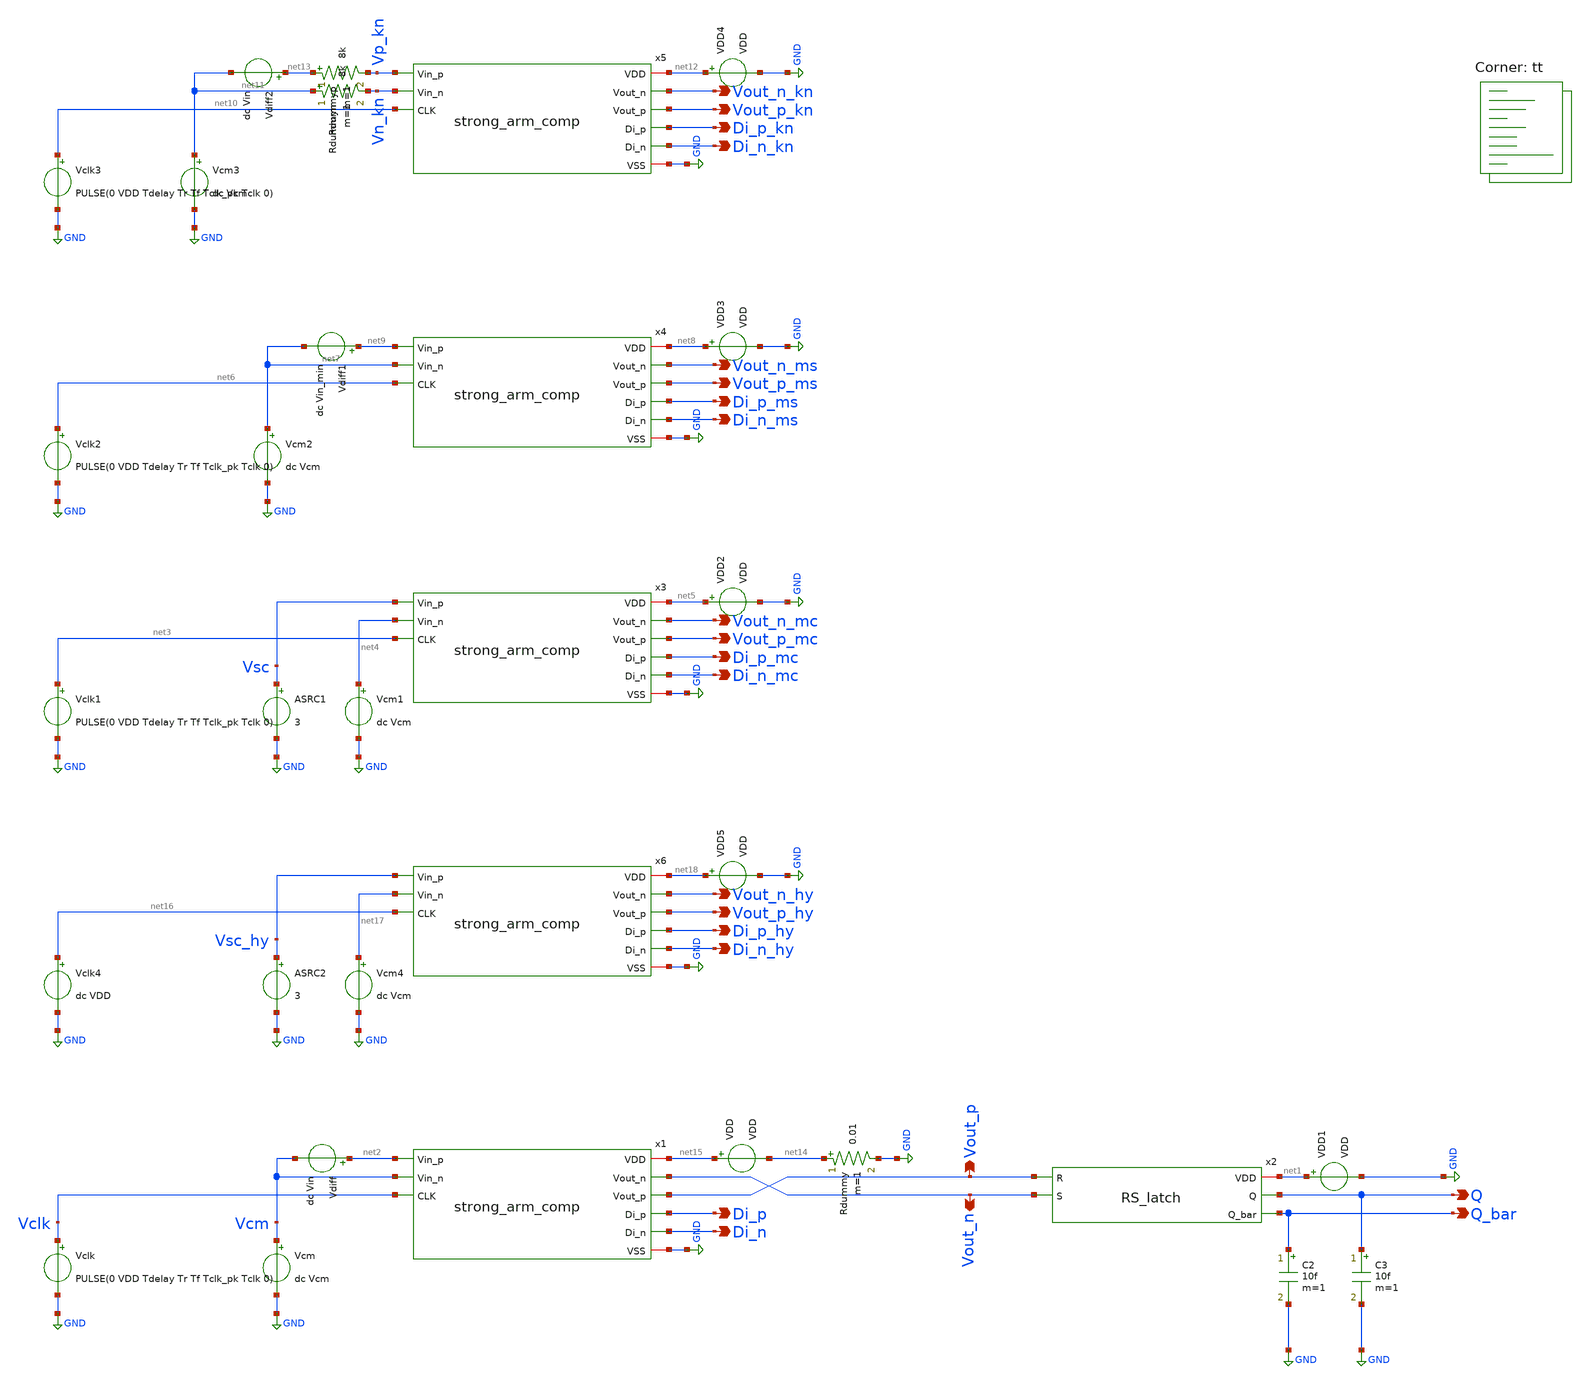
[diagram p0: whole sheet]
** sch_path: xschem/strong_arm_comp_tb.sch
**.subckt strong_arm_comp_tb Vout_n Vout_p Q Q_bar Vout_n_mc Vout_p_mc Vout_n_ms Vout_p_ms Vout_n_kn
*+ Vout_p_kn Vout_n_hy Vout_p_hy Di_p Di_n Di_p_hy Di_n_hy Di_p_ms Di_n_ms Di_p_kn Di_n_kn Di_p_mc Di_n_mc
*.opin Vout_n
*.opin Vout_p
*.opin Q
*.opin Q_bar
*.opin Vout_n_mc
*.opin Vout_p_mc
*.opin Vout_n_ms
*.opin Vout_p_ms
*.opin Vout_n_kn
*.opin Vout_p_kn
*.opin Vout_n_hy
*.opin Vout_p_hy
*.opin Di_p
*.opin Di_n
*.opin Di_p_hy
*.opin Di_n_hy
*.opin Di_p_ms
*.opin Di_n_ms
*.opin Di_p_kn
*.opin Di_n_kn
*.opin Di_p_mc
*.opin Di_n_mc
VDD net15 net14 VDD
Vclk Vclk GND PULSE(0 VDD Tdelay Tr Tf Tclk_pk Tclk 0)
Vcm Vcm GND dc Vcm
Vdiff net2 Vcm dc Vin
C2 Q_bar GND 10f m=1
C3 Q GND 10f m=1
Rdummy net14 GND 0.01 m=1
VDD1 net1 GND VDD
x1 net15 Vout_n Vout_p Di_p Di_n net2 Vcm Vclk GND strong_arm_comp
VDD2 net5 GND VDD
Vclk1 net3 GND PULSE(0 VDD Tdelay Tr Tf Tclk_pk Tclk 0)
Vcm1 net4 GND dc Vcm
x3 net5 Vout_n_mc Vout_p_mc Di_p_mc Di_n_mc Vsc net4 net3 GND strong_arm_comp
ASRC1 %v([ Vsc ]) filesrc
VDD3 net8 GND VDD
Vclk2 net6 GND PULSE(0 VDD Tdelay Tr Tf Tclk_pk Tclk 0)
Vcm2 net7 GND dc Vcm
x4 net8 Vout_n_ms Vout_p_ms Di_p_ms Di_n_ms net9 net7 net6 GND strong_arm_comp
Vdiff1 net9 net7 dc Vin_min
VDD4 net12 GND VDD
Vclk3 net10 GND PULSE(0 VDD Tdelay Tr Tf Tclk_pk Tclk 0)
Vcm3 net11 GND dc Vcm
x5 net12 Vout_n_kn Vout_p_kn Di_p_kn Di_n_kn Vp_kn Vn_kn net10 GND strong_arm_comp
Vdiff2 net13 net11 dc Vin
Rdummyp net13 Vp_kn 8k m=1
Rdummyn net11 Vn_kn 8k m=1
x2 net1 Vout_p Q Vout_n Q_bar RS_latch
VDD5 net18 GND VDD
Vclk4 net16 GND dc VDD
Vcm4 net17 GND dc Vcm
x6 net18 Vout_n_hy Vout_p_hy Di_p_hy Di_n_hy Vsc_hy net17 net16 GND strong_arm_comp
ASRC2 %v([ Vsc_hy ]) filesrc
**** begin user architecture code
.lib $::SKYWATER_MODELS/sky130.lib.spice tt


*.OPTIONS maxord=1
*.OPTIONS itl1=200
*.OPTIONS itl2=200
*.OPTIONS itl4=200

* save all voltage and current
.save all
.options savecurrents
.options seed=random

.nodeset V(Vout_n) = 0
.nodeset V(Vout_p) = 0
.nodeset V(Q) = 0
.nodeset V(Q_bar) = 0

.nodeset V(Vout_n_mc) = 0
.nodeset V(Vout_p_mc) = 0

.nodeset V(Vout_n_ms) = 0
.nodeset V(Vout_p_ms) = 0

*.nodeset V(x6.Di_p) = 1.8
*.nodeset V(x6.Di_n) = 1.62

.control
set filetype=ascii
set units=degrees

.include /autofs/fs1.ece/fs1.eecg.tcc/lizongh2/sky130_comparator/xschem/simulations/strong_arm_comp_tb_vars.spice
.include /autofs/fs1.ece/fs1.eecg.tcc/lizongh2/sky130_comparator/xschem/simulations/strong_arm_comp_tb_analyses.spice

.endc


**** end user architecture code
**.ends

* expanding   symbol:  strong_arm_comp.sym # of pins=9
** sym_path: xschem/strong_arm_comp.sym
** sch_path: xschem/strong_arm_comp.sch
.subckt strong_arm_comp VDD Vout_n Vout_p Di_p Di_n Vin_p Vin_n CLK VSS
*.ipin Vin_p
*.ipin Vin_n
*.ipin CLK
*.iopin VDD
*.opin Vout_n
*.opin Vout_p
*.iopin VSS
*.opin Di_n
*.opin Di_p
XM1 Di_n Vin_p net1 VSS sky130_fd_pr__nfet_01v8 L=0.15 W=W_M1 nf=1 ad='int((nf+1)/2) * W/nf * 0.29' as='int((nf+2)/2) * W/nf * 0.29'
+ pd='2*int((nf+1)/2) * (W/nf + 0.29)' ps='2*int((nf+2)/2) * (W/nf + 0.29)' nrd='0.29 / W' nrs='0.29 / W'
+ sa=0 sb=0 sd=0 mult=1 m=1
XM2 Di_p Vin_n net1 VSS sky130_fd_pr__nfet_01v8 L=0.15 W=W_M2 nf=1 ad='int((nf+1)/2) * W/nf * 0.29' as='int((nf+2)/2) * W/nf * 0.29'
+ pd='2*int((nf+1)/2) * (W/nf + 0.29)' ps='2*int((nf+2)/2) * (W/nf + 0.29)' nrd='0.29 / W' nrs='0.29 / W'
+ sa=0 sb=0 sd=0 mult=1 m=1
XM3 Vout_n Vout_p Di_n VSS sky130_fd_pr__nfet_01v8 L=0.15 W=W_M3 nf=1 ad='int((nf+1)/2) * W/nf * 0.29'
+ as='int((nf+2)/2) * W/nf * 0.29' pd='2*int((nf+1)/2) * (W/nf + 0.29)' ps='2*int((nf+2)/2) * (W/nf + 0.29)'
+ nrd='0.29 / W' nrs='0.29 / W' sa=0 sb=0 sd=0 mult=1 m=1
XM4 Vout_p Vout_n Di_p VSS sky130_fd_pr__nfet_01v8 L=0.15 W=W_M4 nf=1 ad='int((nf+1)/2) * W/nf * 0.29'
+ as='int((nf+2)/2) * W/nf * 0.29' pd='2*int((nf+1)/2) * (W/nf + 0.29)' ps='2*int((nf+2)/2) * (W/nf + 0.29)'
+ nrd='0.29 / W' nrs='0.29 / W' sa=0 sb=0 sd=0 mult=1 m=1
XM5 Vout_n Vout_p VDD VDD sky130_fd_pr__pfet_01v8 L=0.15 W=W_M5 nf=1 ad='int((nf+1)/2) * W/nf * 0.29'
+ as='int((nf+2)/2) * W/nf * 0.29' pd='2*int((nf+1)/2) * (W/nf + 0.29)' ps='2*int((nf+2)/2) * (W/nf + 0.29)'
+ nrd='0.29 / W' nrs='0.29 / W' sa=0 sb=0 sd=0 mult=1 m=1
XM6 Vout_p Vout_n VDD VDD sky130_fd_pr__pfet_01v8 L=0.15 W=W_M6 nf=1 ad='int((nf+1)/2) * W/nf * 0.29'
+ as='int((nf+2)/2) * W/nf * 0.29' pd='2*int((nf+1)/2) * (W/nf + 0.29)' ps='2*int((nf+2)/2) * (W/nf + 0.29)'
+ nrd='0.29 / W' nrs='0.29 / W' sa=0 sb=0 sd=0 mult=1 m=1
XM9 Vout_p CLK VDD VDD sky130_fd_pr__pfet_01v8 L=0.15 W=W_M9 nf=1 ad='int((nf+1)/2) * W/nf * 0.29' as='int((nf+2)/2) * W/nf * 0.29'
+ pd='2*int((nf+1)/2) * (W/nf + 0.29)' ps='2*int((nf+2)/2) * (W/nf + 0.29)' nrd='0.29 / W' nrs='0.29 / W'
+ sa=0 sb=0 sd=0 mult=1 m=1
XM8 Vout_n CLK VDD VDD sky130_fd_pr__pfet_01v8 L=0.15 W=W_M8 nf=1 ad='int((nf+1)/2) * W/nf * 0.29' as='int((nf+2)/2) * W/nf * 0.29'
+ pd='2*int((nf+1)/2) * (W/nf + 0.29)' ps='2*int((nf+2)/2) * (W/nf + 0.29)' nrd='0.29 / W' nrs='0.29 / W'
+ sa=0 sb=0 sd=0 mult=1 m=1
XM7 net1 CLK VSS VSS sky130_fd_pr__nfet_01v8 L=0.15 W=W_M7 nf=1 ad='int((nf+1)/2) * W/nf * 0.29' as='int((nf+2)/2) * W/nf * 0.29'
+ pd='2*int((nf+1)/2) * (W/nf + 0.29)' ps='2*int((nf+2)/2) * (W/nf + 0.29)' nrd='0.29 / W' nrs='0.29 / W'
+ sa=0 sb=0 sd=0 mult=1 m=1
XM10 Di_n CLK VDD VDD sky130_fd_pr__pfet_01v8 L=0.15 W=W_M10 nf=1 ad='int((nf+1)/2) * W/nf * 0.29' as='int((nf+2)/2) * W/nf * 0.29'
+ pd='2*int((nf+1)/2) * (W/nf + 0.29)' ps='2*int((nf+2)/2) * (W/nf + 0.29)' nrd='0.29 / W' nrs='0.29 / W'
+ sa=0 sb=0 sd=0 mult=1 m=1
XM11 Di_p CLK VDD VDD sky130_fd_pr__pfet_01v8 L=0.15 W=W_M11 nf=1 ad='int((nf+1)/2) * W/nf * 0.29' as='int((nf+2)/2) * W/nf * 0.29'
+ pd='2*int((nf+1)/2) * (W/nf + 0.29)' ps='2*int((nf+2)/2) * (W/nf + 0.29)' nrd='0.29 / W' nrs='0.29 / W'
+ sa=0 sb=0 sd=0 mult=1 m=1
.ends


* expanding   symbol:  RS_latch.sym # of pins=5
** sym_path: xschem/RS_latch.sym
** sch_path: xschem/RS_latch.sch
.subckt RS_latch VDD R Q S Q_bar
*.iopin VDD
*.opin Q
*.opin Q_bar
*.ipin R
*.ipin S
x1 VDD R Q_bar Q nor
x2 VDD Q S Q_bar nor
.ends


* expanding   symbol:  nor.sym # of pins=4
** sym_path: xschem/nor.sym
** sch_path: xschem/nor.sch
.subckt nor VDD A B out
*.iopin VDD
*.ipin A
*.ipin B
*.opin out
XM1 out B GND GND sky130_fd_pr__nfet_01v8 L=0.15 W=0.42 nf=1 ad='int((nf+1)/2) * W/nf * 0.29' as='int((nf+2)/2) * W/nf * 0.29'
+ pd='2*int((nf+1)/2) * (W/nf + 0.29)' ps='2*int((nf+2)/2) * (W/nf + 0.29)' nrd='0.29 / W' nrs='0.29 / W'
+ sa=0 sb=0 sd=0 mult=1 m=1
XM2 out A GND GND sky130_fd_pr__nfet_01v8 L=0.15 W=0.42 nf=1 ad='int((nf+1)/2) * W/nf * 0.29' as='int((nf+2)/2) * W/nf * 0.29'
+ pd='2*int((nf+1)/2) * (W/nf + 0.29)' ps='2*int((nf+2)/2) * (W/nf + 0.29)' nrd='0.29 / W' nrs='0.29 / W'
+ sa=0 sb=0 sd=0 mult=1 m=1
XM3 out B net1 VDD sky130_fd_pr__pfet_01v8 L=0.15 W=0.84 nf=1 ad='int((nf+1)/2) * W/nf * 0.29' as='int((nf+2)/2) * W/nf * 0.29'
+ pd='2*int((nf+1)/2) * (W/nf + 0.29)' ps='2*int((nf+2)/2) * (W/nf + 0.29)' nrd='0.29 / W' nrs='0.29 / W'
+ sa=0 sb=0 sd=0 mult=1 m=1
XM4 net1 A VDD VDD sky130_fd_pr__pfet_01v8 L=0.15 W=0.84 nf=1 ad='int((nf+1)/2) * W/nf * 0.29' as='int((nf+2)/2) * W/nf * 0.29'
+ pd='2*int((nf+1)/2) * (W/nf + 0.29)' ps='2*int((nf+2)/2) * (W/nf + 0.29)' nrd='0.29 / W' nrs='0.29 / W'
+ sa=0 sb=0 sd=0 mult=1 m=1
.ends

.GLOBAL GND
**** begin user architecture code

.model filesrc filesource (file="staircase_voltage_hysteresis.txt" amploffset=[Vcm] amplscale=[1]
+ timeoffset=0 timescale=1 timerelative=false amplstep=false)

**** end user architecture code
.end
